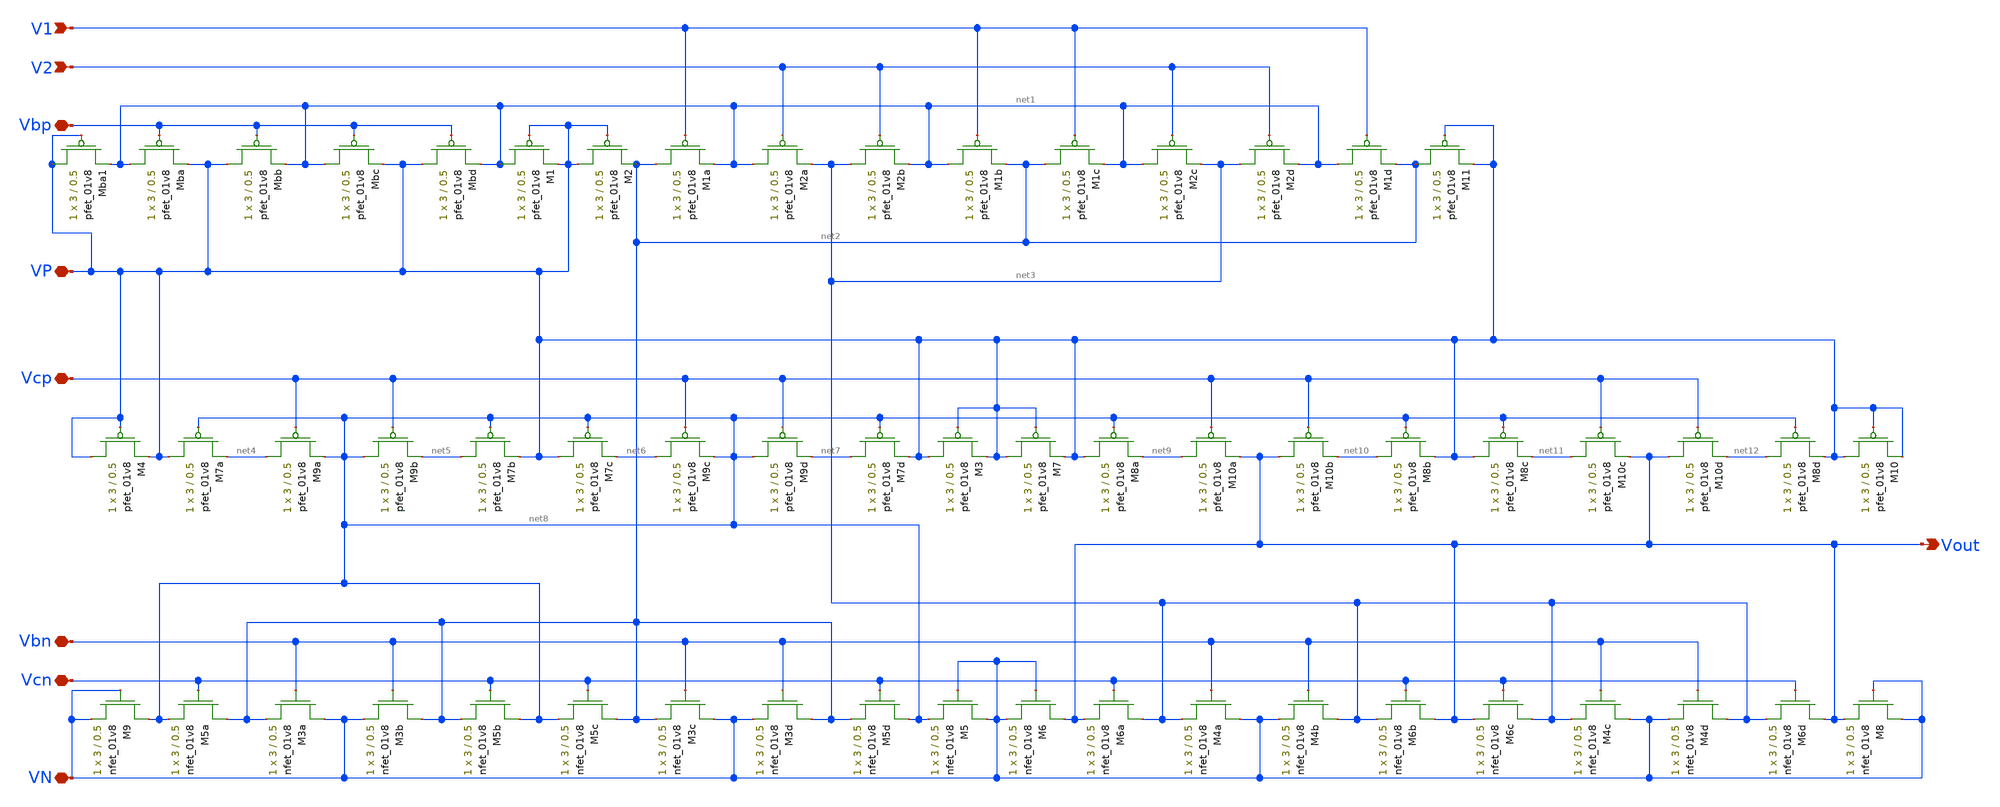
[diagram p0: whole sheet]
** sch_path: Miniproject3/fcdiffamp.sch
**.subckt fcdiffamp Vbn V2 Vout V1 Vcp Vbp Vcn VP VN
*.iopin Vbn
*.ipin V2
*.opin Vout
*.ipin V1
*.iopin Vcp
*.iopin Vbp
*.iopin Vcn
*.iopin VP
*.iopin VN
XM3a VN Vbn net2 GND sky130_fd_pr__nfet_01v8 L=0.5 W=3 nf=1 ad='int((nf+1)/2) * W/nf * 0.29' as='int((nf+2)/2) * W/nf * 0.29'
+ pd='2*int((nf+1)/2) * (W/nf + 0.29)' ps='2*int((nf+2)/2) * (W/nf + 0.29)' nrd='0.29 / W' nrs='0.29 / W'
+ sa=0 sb=0 sd=0 mult=1 m=1
XM4a VN Vbn net3 GND sky130_fd_pr__nfet_01v8 L=0.5 W=3 nf=1 ad='int((nf+1)/2) * W/nf * 0.29' as='int((nf+2)/2) * W/nf * 0.29'
+ pd='2*int((nf+1)/2) * (W/nf + 0.29)' ps='2*int((nf+2)/2) * (W/nf + 0.29)' nrd='0.29 / W' nrs='0.29 / W'
+ sa=0 sb=0 sd=0 mult=1 m=1
XM4b net3 Vbn VN GND sky130_fd_pr__nfet_01v8 L=0.5 W=3 nf=1 ad='int((nf+1)/2) * W/nf * 0.29' as='int((nf+2)/2) * W/nf * 0.29'
+ pd='2*int((nf+1)/2) * (W/nf + 0.29)' ps='2*int((nf+2)/2) * (W/nf + 0.29)' nrd='0.29 / W' nrs='0.29 / W'
+ sa=0 sb=0 sd=0 mult=1 m=1
XM3b net2 Vbn VN GND sky130_fd_pr__nfet_01v8 L=0.5 W=3 nf=1 ad='int((nf+1)/2) * W/nf * 0.29' as='int((nf+2)/2) * W/nf * 0.29'
+ pd='2*int((nf+1)/2) * (W/nf + 0.29)' ps='2*int((nf+2)/2) * (W/nf + 0.29)' nrd='0.29 / W' nrs='0.29 / W'
+ sa=0 sb=0 sd=0 mult=1 m=1
XM3c VN Vbn net2 GND sky130_fd_pr__nfet_01v8 L=0.5 W=3 nf=1 ad='int((nf+1)/2) * W/nf * 0.29' as='int((nf+2)/2) * W/nf * 0.29'
+ pd='2*int((nf+1)/2) * (W/nf + 0.29)' ps='2*int((nf+2)/2) * (W/nf + 0.29)' nrd='0.29 / W' nrs='0.29 / W'
+ sa=0 sb=0 sd=0 mult=1 m=1
XM4c VN Vbn net3 GND sky130_fd_pr__nfet_01v8 L=0.5 W=3 nf=1 ad='int((nf+1)/2) * W/nf * 0.29' as='int((nf+2)/2) * W/nf * 0.29'
+ pd='2*int((nf+1)/2) * (W/nf + 0.29)' ps='2*int((nf+2)/2) * (W/nf + 0.29)' nrd='0.29 / W' nrs='0.29 / W'
+ sa=0 sb=0 sd=0 mult=1 m=1
XM4d net3 Vbn VN GND sky130_fd_pr__nfet_01v8 L=0.5 W=3 nf=1 ad='int((nf+1)/2) * W/nf * 0.29' as='int((nf+2)/2) * W/nf * 0.29'
+ pd='2*int((nf+1)/2) * (W/nf + 0.29)' ps='2*int((nf+2)/2) * (W/nf + 0.29)' nrd='0.29 / W' nrs='0.29 / W'
+ sa=0 sb=0 sd=0 mult=1 m=1
XM3d net2 Vbn VN GND sky130_fd_pr__nfet_01v8 L=0.5 W=3 nf=1 ad='int((nf+1)/2) * W/nf * 0.29' as='int((nf+2)/2) * W/nf * 0.29'
+ pd='2*int((nf+1)/2) * (W/nf + 0.29)' ps='2*int((nf+2)/2) * (W/nf + 0.29)' nrd='0.29 / W' nrs='0.29 / W'
+ sa=0 sb=0 sd=0 mult=1 m=1
XMba net1 Vbp VP VDD sky130_fd_pr__pfet_01v8 L=0.5 W=3 nf=1 ad='int((nf+1)/2) * W/nf * 0.29' as='int((nf+2)/2) * W/nf * 0.29'
+ pd='2*int((nf+1)/2) * (W/nf + 0.29)' ps='2*int((nf+2)/2) * (W/nf + 0.29)' nrd='0.29 / W' nrs='0.29 / W'
+ sa=0 sb=0 sd=0 mult=1 m=1
XMbb VP Vbp net1 VDD sky130_fd_pr__pfet_01v8 L=0.5 W=3 nf=1 ad='int((nf+1)/2) * W/nf * 0.29' as='int((nf+2)/2) * W/nf * 0.29'
+ pd='2*int((nf+1)/2) * (W/nf + 0.29)' ps='2*int((nf+2)/2) * (W/nf + 0.29)' nrd='0.29 / W' nrs='0.29 / W'
+ sa=0 sb=0 sd=0 mult=1 m=1
XMbc net1 Vbp VP VDD sky130_fd_pr__pfet_01v8 L=0.5 W=3 nf=1 ad='int((nf+1)/2) * W/nf * 0.29' as='int((nf+2)/2) * W/nf * 0.29'
+ pd='2*int((nf+1)/2) * (W/nf + 0.29)' ps='2*int((nf+2)/2) * (W/nf + 0.29)' nrd='0.29 / W' nrs='0.29 / W'
+ sa=0 sb=0 sd=0 mult=1 m=1
XMbd VP Vbp net1 VDD sky130_fd_pr__pfet_01v8 L=0.5 W=3 nf=1 ad='int((nf+1)/2) * W/nf * 0.29' as='int((nf+2)/2) * W/nf * 0.29'
+ pd='2*int((nf+1)/2) * (W/nf + 0.29)' ps='2*int((nf+2)/2) * (W/nf + 0.29)' nrd='0.29 / W' nrs='0.29 / W'
+ sa=0 sb=0 sd=0 mult=1 m=1
XM1a net2 V1 net1 VDD sky130_fd_pr__pfet_01v8 L=0.5 W=3 nf=1 ad='int((nf+1)/2) * W/nf * 0.29' as='int((nf+2)/2) * W/nf * 0.29'
+ pd='2*int((nf+1)/2) * (W/nf + 0.29)' ps='2*int((nf+2)/2) * (W/nf + 0.29)' nrd='0.29 / W' nrs='0.29 / W'
+ sa=0 sb=0 sd=0 mult=1 m=1
XM2a net1 V2 net3 VDD sky130_fd_pr__pfet_01v8 L=0.5 W=3 nf=1 ad='int((nf+1)/2) * W/nf * 0.29' as='int((nf+2)/2) * W/nf * 0.29'
+ pd='2*int((nf+1)/2) * (W/nf + 0.29)' ps='2*int((nf+2)/2) * (W/nf + 0.29)' nrd='0.29 / W' nrs='0.29 / W'
+ sa=0 sb=0 sd=0 mult=1 m=1
XM2b net3 V2 net1 VDD sky130_fd_pr__pfet_01v8 L=0.5 W=3 nf=1 ad='int((nf+1)/2) * W/nf * 0.29' as='int((nf+2)/2) * W/nf * 0.29'
+ pd='2*int((nf+1)/2) * (W/nf + 0.29)' ps='2*int((nf+2)/2) * (W/nf + 0.29)' nrd='0.29 / W' nrs='0.29 / W'
+ sa=0 sb=0 sd=0 mult=1 m=1
XM1b net1 V1 net2 VDD sky130_fd_pr__pfet_01v8 L=0.5 W=3 nf=1 ad='int((nf+1)/2) * W/nf * 0.29' as='int((nf+2)/2) * W/nf * 0.29'
+ pd='2*int((nf+1)/2) * (W/nf + 0.29)' ps='2*int((nf+2)/2) * (W/nf + 0.29)' nrd='0.29 / W' nrs='0.29 / W'
+ sa=0 sb=0 sd=0 mult=1 m=1
XM1c net2 V1 net1 VDD sky130_fd_pr__pfet_01v8 L=0.5 W=3 nf=1 ad='int((nf+1)/2) * W/nf * 0.29' as='int((nf+2)/2) * W/nf * 0.29'
+ pd='2*int((nf+1)/2) * (W/nf + 0.29)' ps='2*int((nf+2)/2) * (W/nf + 0.29)' nrd='0.29 / W' nrs='0.29 / W'
+ sa=0 sb=0 sd=0 mult=1 m=1
XM2c net1 V2 net3 VDD sky130_fd_pr__pfet_01v8 L=0.5 W=3 nf=1 ad='int((nf+1)/2) * W/nf * 0.29' as='int((nf+2)/2) * W/nf * 0.29'
+ pd='2*int((nf+1)/2) * (W/nf + 0.29)' ps='2*int((nf+2)/2) * (W/nf + 0.29)' nrd='0.29 / W' nrs='0.29 / W'
+ sa=0 sb=0 sd=0 mult=1 m=1
XM2d net3 V2 net1 VDD sky130_fd_pr__pfet_01v8 L=0.5 W=3 nf=1 ad='int((nf+1)/2) * W/nf * 0.29' as='int((nf+2)/2) * W/nf * 0.29'
+ pd='2*int((nf+1)/2) * (W/nf + 0.29)' ps='2*int((nf+2)/2) * (W/nf + 0.29)' nrd='0.29 / W' nrs='0.29 / W'
+ sa=0 sb=0 sd=0 mult=1 m=1
XM1d net1 V1 net2 VDD sky130_fd_pr__pfet_01v8 L=0.5 W=3 nf=1 ad='int((nf+1)/2) * W/nf * 0.29' as='int((nf+2)/2) * W/nf * 0.29'
+ pd='2*int((nf+1)/2) * (W/nf + 0.29)' ps='2*int((nf+2)/2) * (W/nf + 0.29)' nrd='0.29 / W' nrs='0.29 / W'
+ sa=0 sb=0 sd=0 mult=1 m=1
XM5a net2 Vcn net8 GND sky130_fd_pr__nfet_01v8 L=0.5 W=3 nf=1 ad='int((nf+1)/2) * W/nf * 0.29' as='int((nf+2)/2) * W/nf * 0.29'
+ pd='2*int((nf+1)/2) * (W/nf + 0.29)' ps='2*int((nf+2)/2) * (W/nf + 0.29)' nrd='0.29 / W' nrs='0.29 / W'
+ sa=0 sb=0 sd=0 mult=1 m=1
XM5b net8 Vcn net2 GND sky130_fd_pr__nfet_01v8 L=0.5 W=3 nf=1 ad='int((nf+1)/2) * W/nf * 0.29' as='int((nf+2)/2) * W/nf * 0.29'
+ pd='2*int((nf+1)/2) * (W/nf + 0.29)' ps='2*int((nf+2)/2) * (W/nf + 0.29)' nrd='0.29 / W' nrs='0.29 / W'
+ sa=0 sb=0 sd=0 mult=1 m=1
XM5c net2 Vcn net8 GND sky130_fd_pr__nfet_01v8 L=0.5 W=3 nf=1 ad='int((nf+1)/2) * W/nf * 0.29' as='int((nf+2)/2) * W/nf * 0.29'
+ pd='2*int((nf+1)/2) * (W/nf + 0.29)' ps='2*int((nf+2)/2) * (W/nf + 0.29)' nrd='0.29 / W' nrs='0.29 / W'
+ sa=0 sb=0 sd=0 mult=1 m=1
XM5d net8 Vcn net2 GND sky130_fd_pr__nfet_01v8 L=0.5 W=3 nf=1 ad='int((nf+1)/2) * W/nf * 0.29' as='int((nf+2)/2) * W/nf * 0.29'
+ pd='2*int((nf+1)/2) * (W/nf + 0.29)' ps='2*int((nf+2)/2) * (W/nf + 0.29)' nrd='0.29 / W' nrs='0.29 / W'
+ sa=0 sb=0 sd=0 mult=1 m=1
XM8a VP net8 net9 VDD sky130_fd_pr__pfet_01v8 L=0.5 W=3 nf=1 ad='int((nf+1)/2) * W/nf * 0.29' as='int((nf+2)/2) * W/nf * 0.29'
+ pd='2*int((nf+1)/2) * (W/nf + 0.29)' ps='2*int((nf+2)/2) * (W/nf + 0.29)' nrd='0.29 / W' nrs='0.29 / W'
+ sa=0 sb=0 sd=0 mult=1 m=1
XM10a net9 Vcp Vout VDD sky130_fd_pr__pfet_01v8 L=0.5 W=3 nf=1 ad='int((nf+1)/2) * W/nf * 0.29' as='int((nf+2)/2) * W/nf * 0.29'
+ pd='2*int((nf+1)/2) * (W/nf + 0.29)' ps='2*int((nf+2)/2) * (W/nf + 0.29)' nrd='0.29 / W' nrs='0.29 / W'
+ sa=0 sb=0 sd=0 mult=1 m=1
XM6a net3 Vcn Vout GND sky130_fd_pr__nfet_01v8 L=0.5 W=3 nf=1 ad='int((nf+1)/2) * W/nf * 0.29' as='int((nf+2)/2) * W/nf * 0.29'
+ pd='2*int((nf+1)/2) * (W/nf + 0.29)' ps='2*int((nf+2)/2) * (W/nf + 0.29)' nrd='0.29 / W' nrs='0.29 / W'
+ sa=0 sb=0 sd=0 mult=1 m=1
XM6b Vout Vcn net3 GND sky130_fd_pr__nfet_01v8 L=0.5 W=3 nf=1 ad='int((nf+1)/2) * W/nf * 0.29' as='int((nf+2)/2) * W/nf * 0.29'
+ pd='2*int((nf+1)/2) * (W/nf + 0.29)' ps='2*int((nf+2)/2) * (W/nf + 0.29)' nrd='0.29 / W' nrs='0.29 / W'
+ sa=0 sb=0 sd=0 mult=1 m=1
XM10b Vout Vcp net10 VDD sky130_fd_pr__pfet_01v8 L=0.5 W=3 nf=1 ad='int((nf+1)/2) * W/nf * 0.29' as='int((nf+2)/2) * W/nf * 0.29'
+ pd='2*int((nf+1)/2) * (W/nf + 0.29)' ps='2*int((nf+2)/2) * (W/nf + 0.29)' nrd='0.29 / W' nrs='0.29 / W'
+ sa=0 sb=0 sd=0 mult=1 m=1
XM8b net10 net8 VP VDD sky130_fd_pr__pfet_01v8 L=0.5 W=3 nf=1 ad='int((nf+1)/2) * W/nf * 0.29' as='int((nf+2)/2) * W/nf * 0.29'
+ pd='2*int((nf+1)/2) * (W/nf + 0.29)' ps='2*int((nf+2)/2) * (W/nf + 0.29)' nrd='0.29 / W' nrs='0.29 / W'
+ sa=0 sb=0 sd=0 mult=1 m=1
XM8c VP net8 net11 VDD sky130_fd_pr__pfet_01v8 L=0.5 W=3 nf=1 ad='int((nf+1)/2) * W/nf * 0.29' as='int((nf+2)/2) * W/nf * 0.29'
+ pd='2*int((nf+1)/2) * (W/nf + 0.29)' ps='2*int((nf+2)/2) * (W/nf + 0.29)' nrd='0.29 / W' nrs='0.29 / W'
+ sa=0 sb=0 sd=0 mult=1 m=1
XM10c net11 Vcp Vout VDD sky130_fd_pr__pfet_01v8 L=0.5 W=3 nf=1 ad='int((nf+1)/2) * W/nf * 0.29' as='int((nf+2)/2) * W/nf * 0.29'
+ pd='2*int((nf+1)/2) * (W/nf + 0.29)' ps='2*int((nf+2)/2) * (W/nf + 0.29)' nrd='0.29 / W' nrs='0.29 / W'
+ sa=0 sb=0 sd=0 mult=1 m=1
XM6c net3 Vcn Vout GND sky130_fd_pr__nfet_01v8 L=0.5 W=3 nf=1 ad='int((nf+1)/2) * W/nf * 0.29' as='int((nf+2)/2) * W/nf * 0.29'
+ pd='2*int((nf+1)/2) * (W/nf + 0.29)' ps='2*int((nf+2)/2) * (W/nf + 0.29)' nrd='0.29 / W' nrs='0.29 / W'
+ sa=0 sb=0 sd=0 mult=1 m=1
XM6d Vout Vcn net3 GND sky130_fd_pr__nfet_01v8 L=0.5 W=3 nf=1 ad='int((nf+1)/2) * W/nf * 0.29' as='int((nf+2)/2) * W/nf * 0.29'
+ pd='2*int((nf+1)/2) * (W/nf + 0.29)' ps='2*int((nf+2)/2) * (W/nf + 0.29)' nrd='0.29 / W' nrs='0.29 / W'
+ sa=0 sb=0 sd=0 mult=1 m=1
XM10d Vout Vcp net12 VDD sky130_fd_pr__pfet_01v8 L=0.5 W=3 nf=1 ad='int((nf+1)/2) * W/nf * 0.29' as='int((nf+2)/2) * W/nf * 0.29'
+ pd='2*int((nf+1)/2) * (W/nf + 0.29)' ps='2*int((nf+2)/2) * (W/nf + 0.29)' nrd='0.29 / W' nrs='0.29 / W'
+ sa=0 sb=0 sd=0 mult=1 m=1
XM8d net12 net8 VP VDD sky130_fd_pr__pfet_01v8 L=0.5 W=3 nf=1 ad='int((nf+1)/2) * W/nf * 0.29' as='int((nf+2)/2) * W/nf * 0.29'
+ pd='2*int((nf+1)/2) * (W/nf + 0.29)' ps='2*int((nf+2)/2) * (W/nf + 0.29)' nrd='0.29 / W' nrs='0.29 / W'
+ sa=0 sb=0 sd=0 mult=1 m=1
XM8 VN VN Vout GND sky130_fd_pr__nfet_01v8 L=0.5 W=3 nf=1 ad='int((nf+1)/2) * W/nf * 0.29' as='int((nf+2)/2) * W/nf * 0.29'
+ pd='2*int((nf+1)/2) * (W/nf + 0.29)' ps='2*int((nf+2)/2) * (W/nf + 0.29)' nrd='0.29 / W' nrs='0.29 / W'
+ sa=0 sb=0 sd=0 mult=1 m=1
XM7a VP net8 net4 VDD sky130_fd_pr__pfet_01v8 L=0.5 W=3 nf=1 ad='int((nf+1)/2) * W/nf * 0.29' as='int((nf+2)/2) * W/nf * 0.29'
+ pd='2*int((nf+1)/2) * (W/nf + 0.29)' ps='2*int((nf+2)/2) * (W/nf + 0.29)' nrd='0.29 / W' nrs='0.29 / W'
+ sa=0 sb=0 sd=0 mult=1 m=1
XM9a net4 Vcp net8 VDD sky130_fd_pr__pfet_01v8 L=0.5 W=3 nf=1 ad='int((nf+1)/2) * W/nf * 0.29' as='int((nf+2)/2) * W/nf * 0.29'
+ pd='2*int((nf+1)/2) * (W/nf + 0.29)' ps='2*int((nf+2)/2) * (W/nf + 0.29)' nrd='0.29 / W' nrs='0.29 / W'
+ sa=0 sb=0 sd=0 mult=1 m=1
XM9b net8 Vcp net5 VDD sky130_fd_pr__pfet_01v8 L=0.5 W=3 nf=1 ad='int((nf+1)/2) * W/nf * 0.29' as='int((nf+2)/2) * W/nf * 0.29'
+ pd='2*int((nf+1)/2) * (W/nf + 0.29)' ps='2*int((nf+2)/2) * (W/nf + 0.29)' nrd='0.29 / W' nrs='0.29 / W'
+ sa=0 sb=0 sd=0 mult=1 m=1
XM7b net5 net8 VP VDD sky130_fd_pr__pfet_01v8 L=0.5 W=3 nf=1 ad='int((nf+1)/2) * W/nf * 0.29' as='int((nf+2)/2) * W/nf * 0.29'
+ pd='2*int((nf+1)/2) * (W/nf + 0.29)' ps='2*int((nf+2)/2) * (W/nf + 0.29)' nrd='0.29 / W' nrs='0.29 / W'
+ sa=0 sb=0 sd=0 mult=1 m=1
XM7c VP net8 net6 VDD sky130_fd_pr__pfet_01v8 L=0.5 W=3 nf=1 ad='int((nf+1)/2) * W/nf * 0.29' as='int((nf+2)/2) * W/nf * 0.29'
+ pd='2*int((nf+1)/2) * (W/nf + 0.29)' ps='2*int((nf+2)/2) * (W/nf + 0.29)' nrd='0.29 / W' nrs='0.29 / W'
+ sa=0 sb=0 sd=0 mult=1 m=1
XM9c net6 Vcp net8 VDD sky130_fd_pr__pfet_01v8 L=0.5 W=3 nf=1 ad='int((nf+1)/2) * W/nf * 0.29' as='int((nf+2)/2) * W/nf * 0.29'
+ pd='2*int((nf+1)/2) * (W/nf + 0.29)' ps='2*int((nf+2)/2) * (W/nf + 0.29)' nrd='0.29 / W' nrs='0.29 / W'
+ sa=0 sb=0 sd=0 mult=1 m=1
XM9d net8 Vcp net7 VDD sky130_fd_pr__pfet_01v8 L=0.5 W=3 nf=1 ad='int((nf+1)/2) * W/nf * 0.29' as='int((nf+2)/2) * W/nf * 0.29'
+ pd='2*int((nf+1)/2) * (W/nf + 0.29)' ps='2*int((nf+2)/2) * (W/nf + 0.29)' nrd='0.29 / W' nrs='0.29 / W'
+ sa=0 sb=0 sd=0 mult=1 m=1
XM7d net7 net8 VP VDD sky130_fd_pr__pfet_01v8 L=0.5 W=3 nf=1 ad='int((nf+1)/2) * W/nf * 0.29' as='int((nf+2)/2) * W/nf * 0.29'
+ pd='2*int((nf+1)/2) * (W/nf + 0.29)' ps='2*int((nf+2)/2) * (W/nf + 0.29)' nrd='0.29 / W' nrs='0.29 / W'
+ sa=0 sb=0 sd=0 mult=1 m=1
XM3 VP VP VP VDD sky130_fd_pr__pfet_01v8 L=0.5 W=3 nf=1 ad='int((nf+1)/2) * W/nf * 0.29' as='int((nf+2)/2) * W/nf * 0.29'
+ pd='2*int((nf+1)/2) * (W/nf + 0.29)' ps='2*int((nf+2)/2) * (W/nf + 0.29)' nrd='0.29 / W' nrs='0.29 / W'
+ sa=0 sb=0 sd=0 mult=1 m=1
XM4 VP VP VP VDD sky130_fd_pr__pfet_01v8 L=0.5 W=3 nf=1 ad='int((nf+1)/2) * W/nf * 0.29' as='int((nf+2)/2) * W/nf * 0.29'
+ pd='2*int((nf+1)/2) * (W/nf + 0.29)' ps='2*int((nf+2)/2) * (W/nf + 0.29)' nrd='0.29 / W' nrs='0.29 / W'
+ sa=0 sb=0 sd=0 mult=1 m=1
XM7 VP VP VP VDD sky130_fd_pr__pfet_01v8 L=0.5 W=3 nf=1 ad='int((nf+1)/2) * W/nf * 0.29' as='int((nf+2)/2) * W/nf * 0.29'
+ pd='2*int((nf+1)/2) * (W/nf + 0.29)' ps='2*int((nf+2)/2) * (W/nf + 0.29)' nrd='0.29 / W' nrs='0.29 / W'
+ sa=0 sb=0 sd=0 mult=1 m=1
XM1 net1 VP VP VDD sky130_fd_pr__pfet_01v8 L=0.5 W=3 nf=1 ad='int((nf+1)/2) * W/nf * 0.29' as='int((nf+2)/2) * W/nf * 0.29'
+ pd='2*int((nf+1)/2) * (W/nf + 0.29)' ps='2*int((nf+2)/2) * (W/nf + 0.29)' nrd='0.29 / W' nrs='0.29 / W'
+ sa=0 sb=0 sd=0 mult=1 m=1
XM2 VP VP net2 VDD sky130_fd_pr__pfet_01v8 L=0.5 W=3 nf=1 ad='int((nf+1)/2) * W/nf * 0.29' as='int((nf+2)/2) * W/nf * 0.29'
+ pd='2*int((nf+1)/2) * (W/nf + 0.29)' ps='2*int((nf+2)/2) * (W/nf + 0.29)' nrd='0.29 / W' nrs='0.29 / W'
+ sa=0 sb=0 sd=0 mult=1 m=1
XM5 VN VN net8 GND sky130_fd_pr__nfet_01v8 L=0.5 W=3 nf=1 ad='int((nf+1)/2) * W/nf * 0.29' as='int((nf+2)/2) * W/nf * 0.29'
+ pd='2*int((nf+1)/2) * (W/nf + 0.29)' ps='2*int((nf+2)/2) * (W/nf + 0.29)' nrd='0.29 / W' nrs='0.29 / W'
+ sa=0 sb=0 sd=0 mult=1 m=1
XM6 Vout VN VN GND sky130_fd_pr__nfet_01v8 L=0.5 W=3 nf=1 ad='int((nf+1)/2) * W/nf * 0.29' as='int((nf+2)/2) * W/nf * 0.29'
+ pd='2*int((nf+1)/2) * (W/nf + 0.29)' ps='2*int((nf+2)/2) * (W/nf + 0.29)' nrd='0.29 / W' nrs='0.29 / W'
+ sa=0 sb=0 sd=0 mult=1 m=1
XM9 net8 VN VN GND sky130_fd_pr__nfet_01v8 L=0.5 W=3 nf=1 ad='int((nf+1)/2) * W/nf * 0.29' as='int((nf+2)/2) * W/nf * 0.29'
+ pd='2*int((nf+1)/2) * (W/nf + 0.29)' ps='2*int((nf+2)/2) * (W/nf + 0.29)' nrd='0.29 / W' nrs='0.29 / W'
+ sa=0 sb=0 sd=0 mult=1 m=1
XM10 VP VP VP VDD sky130_fd_pr__pfet_01v8 L=0.5 W=3 nf=1 ad='int((nf+1)/2) * W/nf * 0.29' as='int((nf+2)/2) * W/nf * 0.29'
+ pd='2*int((nf+1)/2) * (W/nf + 0.29)' ps='2*int((nf+2)/2) * (W/nf + 0.29)' nrd='0.29 / W' nrs='0.29 / W'
+ sa=0 sb=0 sd=0 mult=1 m=1
XM11 net2 VP VP VDD sky130_fd_pr__pfet_01v8 L=0.5 W=3 nf=1 ad='int((nf+1)/2) * W/nf * 0.29' as='int((nf+2)/2) * W/nf * 0.29'
+ pd='2*int((nf+1)/2) * (W/nf + 0.29)' ps='2*int((nf+2)/2) * (W/nf + 0.29)' nrd='0.29 / W' nrs='0.29 / W'
+ sa=0 sb=0 sd=0 mult=1 m=1
XMba1 VP VP net1 VDD sky130_fd_pr__pfet_01v8 L=0.5 W=3 nf=1 ad='int((nf+1)/2) * W/nf * 0.29' as='int((nf+2)/2) * W/nf * 0.29'
+ pd='2*int((nf+1)/2) * (W/nf + 0.29)' ps='2*int((nf+2)/2) * (W/nf + 0.29)' nrd='0.29 / W' nrs='0.29 / W'
+ sa=0 sb=0 sd=0 mult=1 m=1
**.ends
.end
